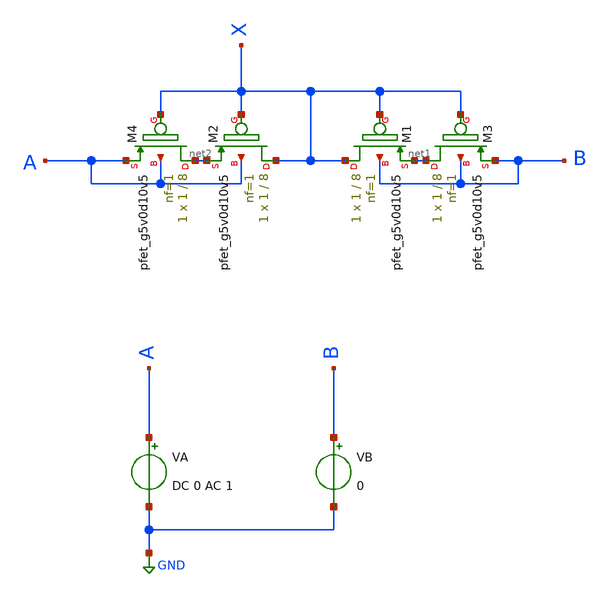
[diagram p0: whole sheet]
** sch_path: xschem/MISC/pseudo/pseudo_tb.sch
* Copyright 2020 Stefan Frederik Schippers
* Licensed under the Apache License, Version 2.0 (the "License");
* you may not use this file except in compliance with the License.
* You may obtain a copy of the License at
* https://www.apache.org/licenses/LICENSE-2.0
* Unless required by applicable law or agreed to in writing, software
* distributed under the License is distributed on an "AS IS" BASIS,
* WITHOUT WARRANTIES OR CONDITIONS OF ANY KIND, either express or implied.
* See the License for the specific language governing permissions and
* limitations under the License.
**.subckt pseudo_tb
XM1 X X net1 B sky130_fd_pr__pfet_g5v0d10v5 L=8 W=1 nf=1 ad='int((nf+1)/2) * W/nf * 0.29' as='int((nf+2)/2) * W/nf * 0.29'
+ pd='2*int((nf+1)/2) * (W/nf + 0.29)' ps='2*int((nf+2)/2) * (W/nf + 0.29)' nrd='0.29 / W' nrs='0.29 / W'
+ sa=0 sb=0 sd=0 mult=1 m=1
XM2 X X net2 A sky130_fd_pr__pfet_g5v0d10v5 L=8 W=1 nf=1 ad='int((nf+1)/2) * W/nf * 0.29' as='int((nf+2)/2) * W/nf * 0.29'
+ pd='2*int((nf+1)/2) * (W/nf + 0.29)' ps='2*int((nf+2)/2) * (W/nf + 0.29)' nrd='0.29 / W' nrs='0.29 / W'
+ sa=0 sb=0 sd=0 mult=1 m=1
VA A GND DC 0 AC 1
VB B GND 0
XM3 net1 X B B sky130_fd_pr__pfet_g5v0d10v5 L=8 W=1 nf=1 ad='int((nf+1)/2) * W/nf * 0.29' as='int((nf+2)/2) * W/nf * 0.29'
+ pd='2*int((nf+1)/2) * (W/nf + 0.29)' ps='2*int((nf+2)/2) * (W/nf + 0.29)' nrd='0.29 / W' nrs='0.29 / W'
+ sa=0 sb=0 sd=0 mult=1 m=1
XM4 net2 X A A sky130_fd_pr__pfet_g5v0d10v5 L=8 W=1 nf=1 ad='int((nf+1)/2) * W/nf * 0.29' as='int((nf+2)/2) * W/nf * 0.29'
+ pd='2*int((nf+1)/2) * (W/nf + 0.29)' ps='2*int((nf+2)/2) * (W/nf + 0.29)' nrd='0.29 / W' nrs='0.29 / W'
+ sa=0 sb=0 sd=0 mult=1 m=1
**** begin user architecture code



.include /usr/share/pdk/sky130A/libs.ref/spi/sky130_fd_pr/sky130_fd_pr__pfet_g5v0d10v5__tt.corner.spice
.include /usr/share/pdk/sky130A/libs.ref/spi/sky130_fd_pr/sky130_fd_pr__pfet_g5v0d10v5__mismatch.corner.spice
.include /usr/share/pdk/sky130A/libs.ref/spi/sky130_fd_pr/sky130_fd_pr__nfet_g5v0d10v5__tt.corner.spice
.include /usr/share/pdk/sky130A/libs.ref/spi/sky130_fd_pr/sky130_fd_pr__nfet_g5v0d10v5__mismatch.corner.spice

.include /usr/share/pdk/sky130A/libs.ref/spi/sky130_fd_pr/sky130_fd_pr__nfet_01v8_lvt__tt.corner.spice
.include /usr/share/pdk/sky130A/libs.ref/spi/sky130_fd_pr/sky130_fd_pr__nfet_01v8_lvt__mismatch.corner.spice
.include /usr/share/pdk/sky130A/libs.ref/spi/sky130_fd_pr/sky130_fd_pr__pfet_01v8_lvt__tt.corner.spice
.include /usr/share/pdk/sky130A/libs.ref/spi/sky130_fd_pr/sky130_fd_pr__pfet_01v8_lvt__mismatch.corner.spice

.include /usr/share/pdk/sky130A/libs.tech/ngspice/all.spice





.param mc_mm_switch=0

.options gmin=1e-16
*.options rshunt = 1.0e14

.control
*  dc VA -0.1 0.1 10.1m
*  let r=abs(deriv(v(a))/deriv(i(va)))
*  plot r ylog

  op
  ac DEC 1 1 1
  print 1/abs(I(VA))

.endc


**** end user architecture code
**.ends
.GLOBAL GND
.end
